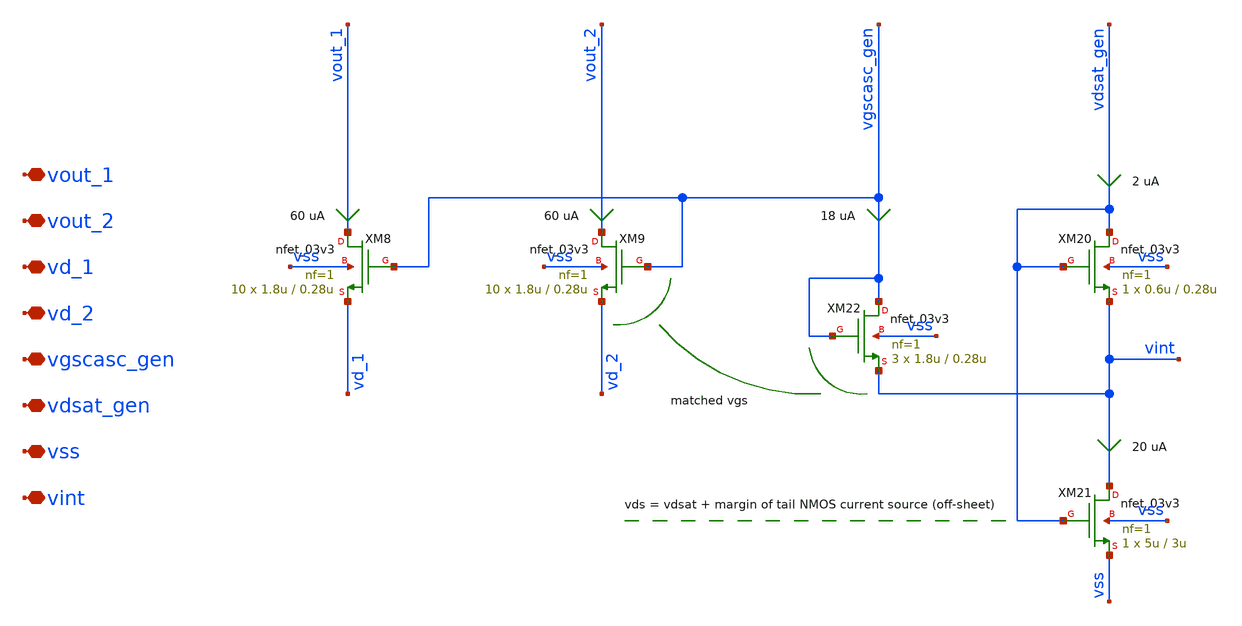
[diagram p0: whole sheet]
** sch_path: xschem/ccia_main_ota/b9_ccia_main_ota_s1_nmos_casc.sch
**.subckt b9_ccia_main_ota_s1_nmos_casc vout_1 vout_2 vd_1 vd_2 vgscasc_gen vdsat_gen vss vint
*.iopin vout_1
*.iopin vout_2
*.iopin vd_1
*.iopin vd_2
*.iopin vgscasc_gen
*.iopin vdsat_gen
*.iopin vss
*.iopin vint
XM9 vout_2 vgscasc_gen vd_2 vss nfet_03v3 L=0.28u W=1.8u nf=1 ad='int((nf+1)/2) * W/nf * 0.18u' as='int((nf+2)/2) * W/nf * 0.18u'
+ pd='2*int((nf+1)/2) * (W/nf + 0.18u)' ps='2*int((nf+2)/2) * (W/nf + 0.18u)' nrd='0.18u / W' nrs='0.18u / W'
+ sa=0 sb=0 sd=0 m=10
XM22 vgscasc_gen vgscasc_gen vint vss nfet_03v3 L=0.28u W=1.8u nf=1 ad='int((nf+1)/2) * W/nf * 0.18u'
+ as='int((nf+2)/2) * W/nf * 0.18u' pd='2*int((nf+1)/2) * (W/nf + 0.18u)' ps='2*int((nf+2)/2) * (W/nf + 0.18u)'
+ nrd='0.18u / W' nrs='0.18u / W' sa=0 sb=0 sd=0 m=3
XM21 vint vdsat_gen vss vss nfet_03v3 L=3u W=5u nf=1 ad='int((nf+1)/2) * W/nf * 0.18u' as='int((nf+2)/2) * W/nf * 0.18u'
+ pd='2*int((nf+1)/2) * (W/nf + 0.18u)' ps='2*int((nf+2)/2) * (W/nf + 0.18u)' nrd='0.18u / W' nrs='0.18u / W'
+ sa=0 sb=0 sd=0 m=1
XM8 vout_1 vgscasc_gen vd_1 vss nfet_03v3 L=0.28u W=1.8u nf=1 ad='int((nf+1)/2) * W/nf * 0.18u' as='int((nf+2)/2) * W/nf * 0.18u'
+ pd='2*int((nf+1)/2) * (W/nf + 0.18u)' ps='2*int((nf+2)/2) * (W/nf + 0.18u)' nrd='0.18u / W' nrs='0.18u / W'
+ sa=0 sb=0 sd=0 m=10
XM20 vdsat_gen vdsat_gen vint vss nfet_03v3 L=0.28u W=0.6u nf=1 ad='int((nf+1)/2) * W/nf * 0.18u' as='int((nf+2)/2) * W/nf * 0.18u'
+ pd='2*int((nf+1)/2) * (W/nf + 0.18u)' ps='2*int((nf+2)/2) * (W/nf + 0.18u)' nrd='0.18u / W' nrs='0.18u / W'
+ sa=0 sb=0 sd=0 m=1
**.ends
.end
